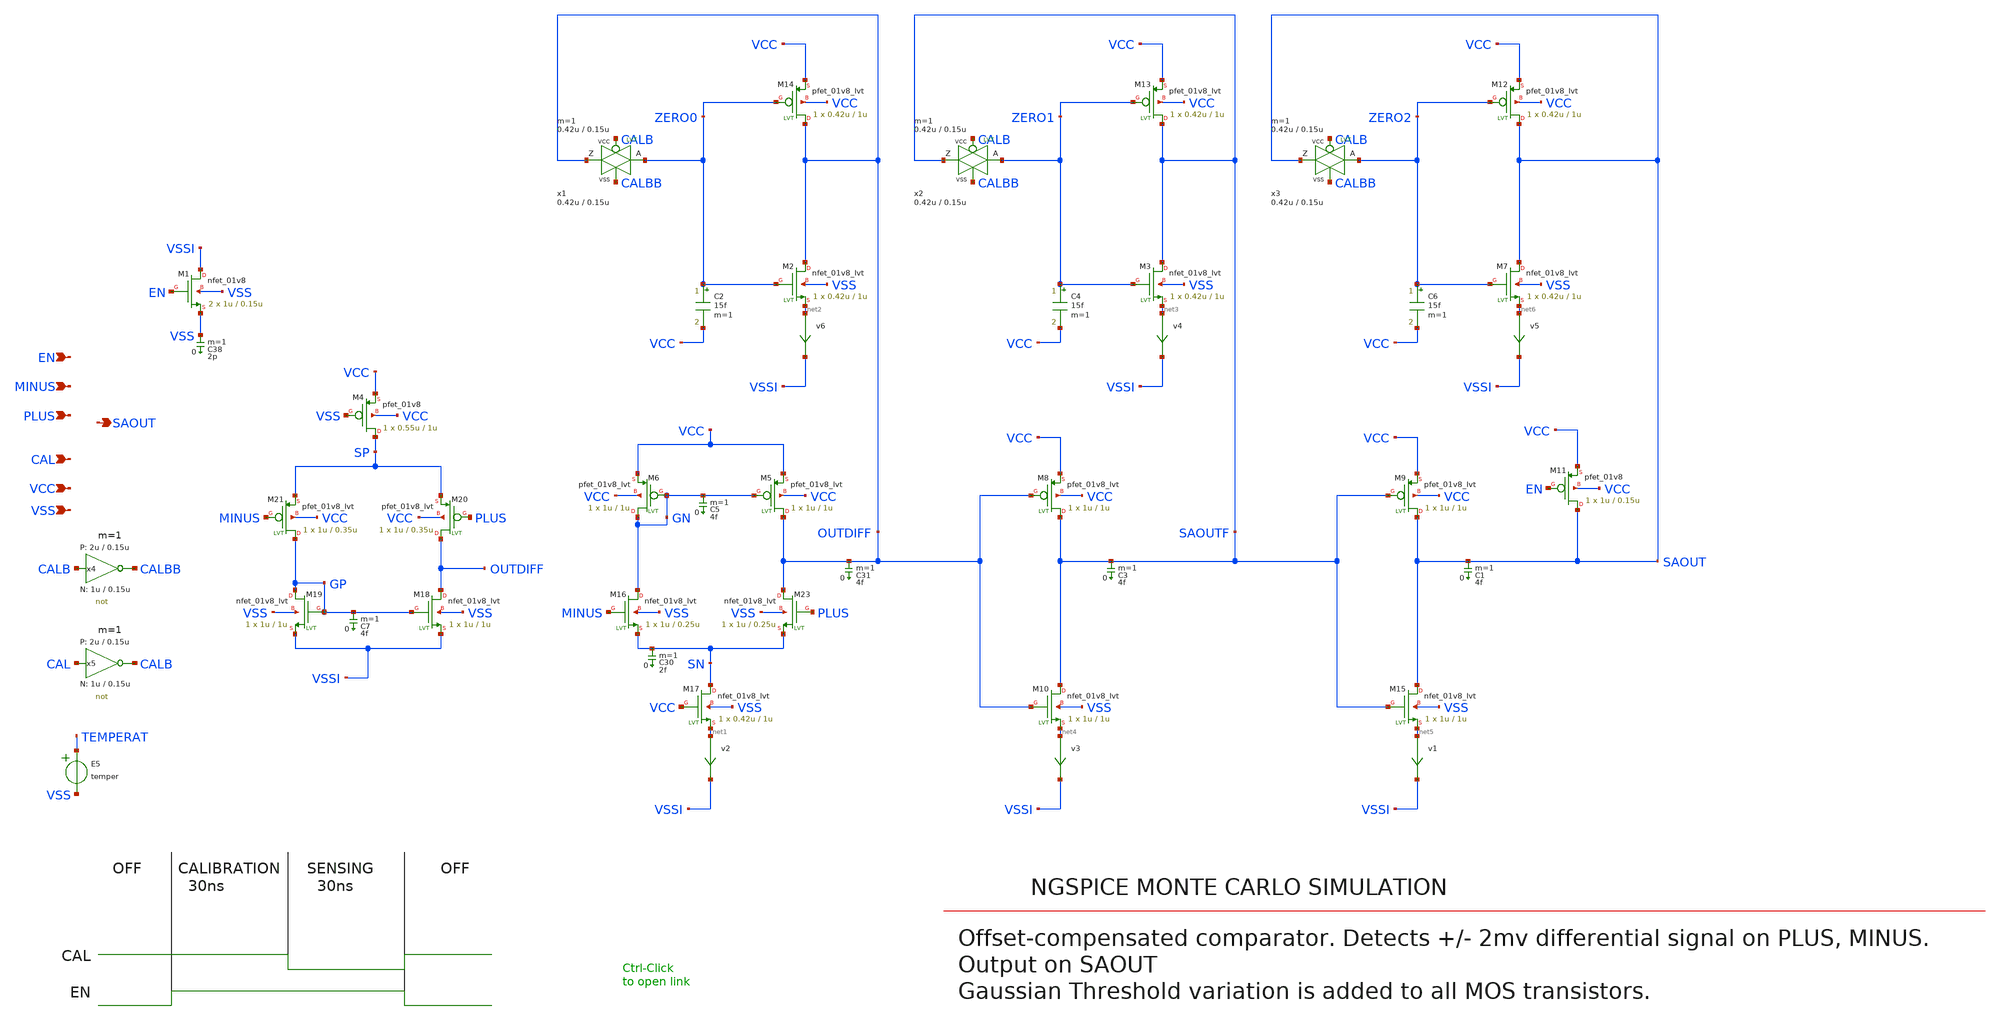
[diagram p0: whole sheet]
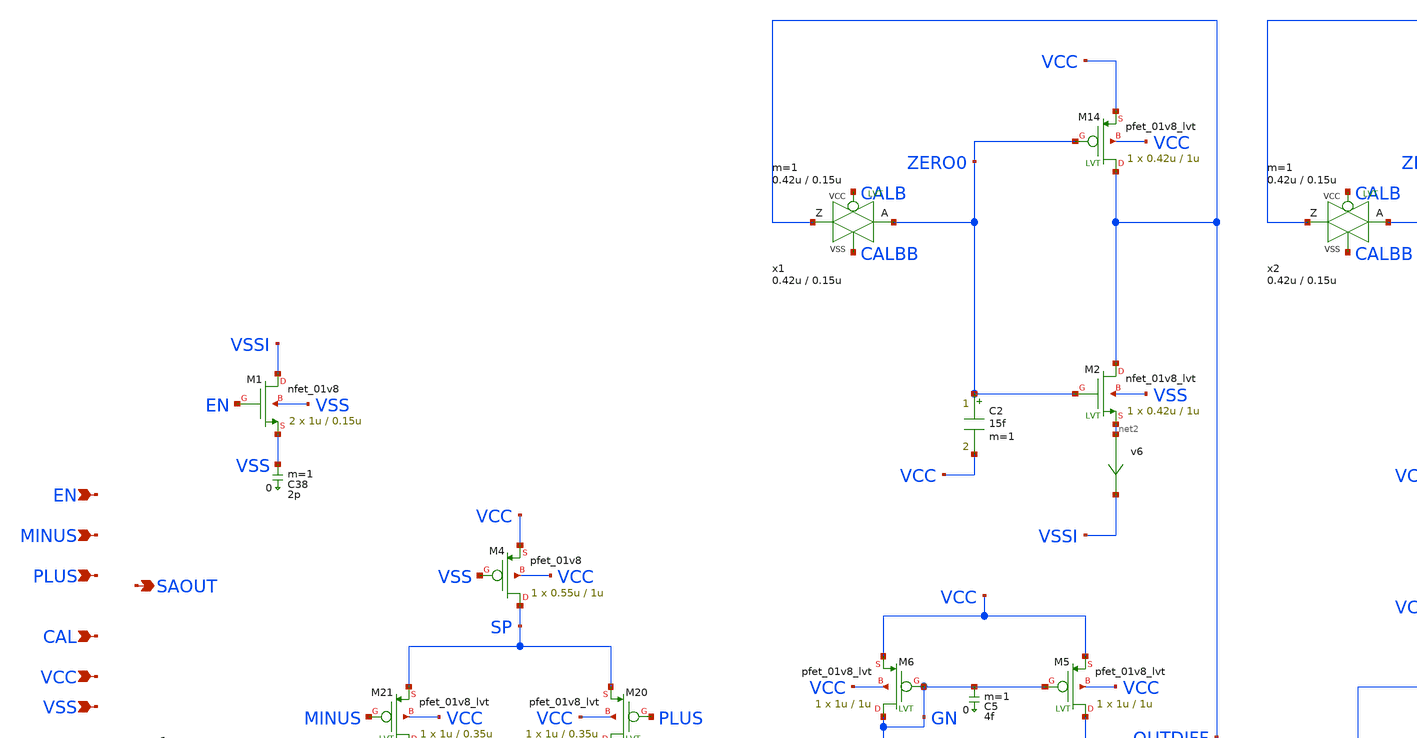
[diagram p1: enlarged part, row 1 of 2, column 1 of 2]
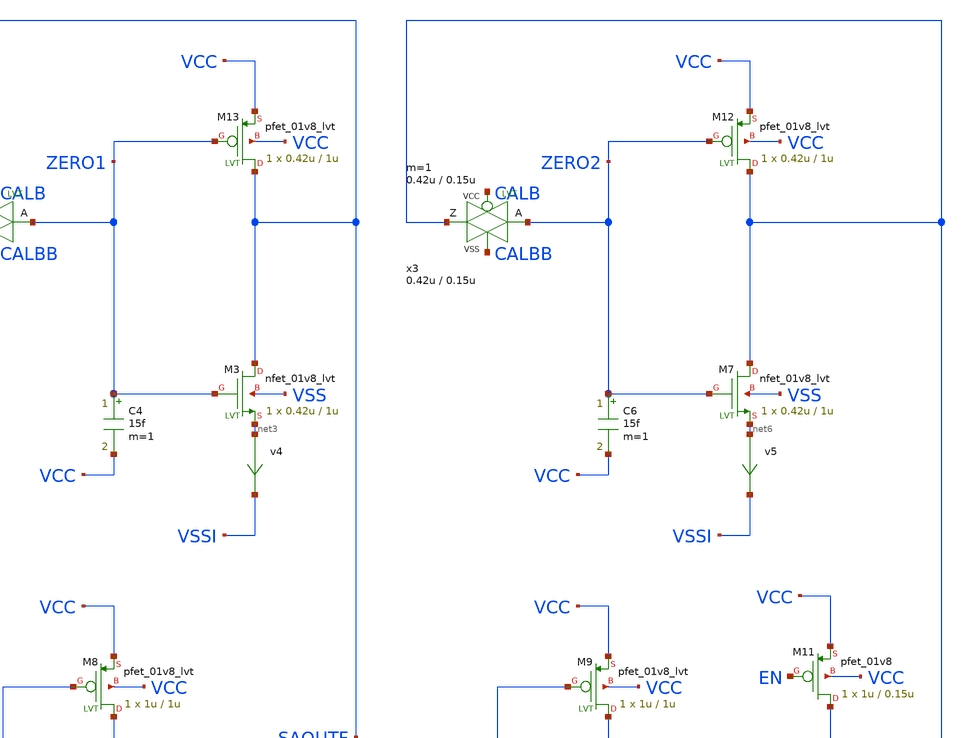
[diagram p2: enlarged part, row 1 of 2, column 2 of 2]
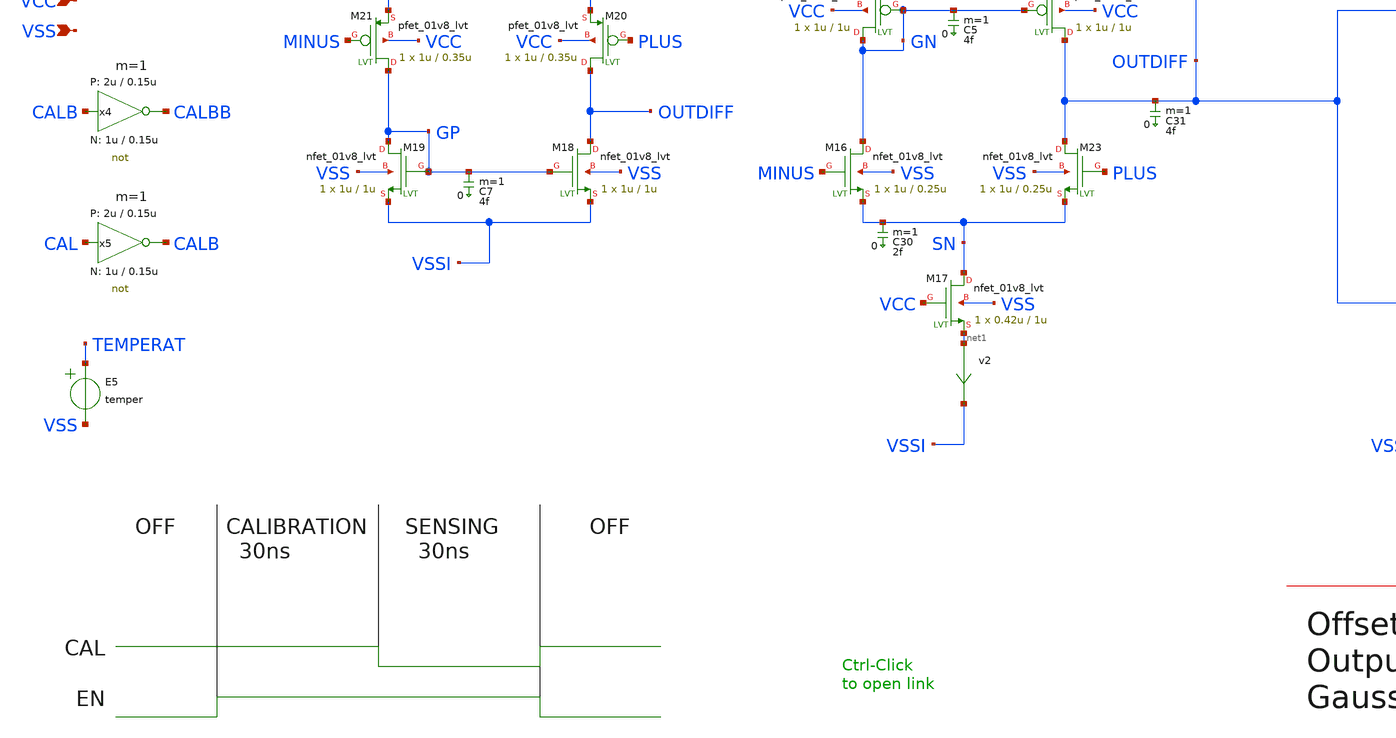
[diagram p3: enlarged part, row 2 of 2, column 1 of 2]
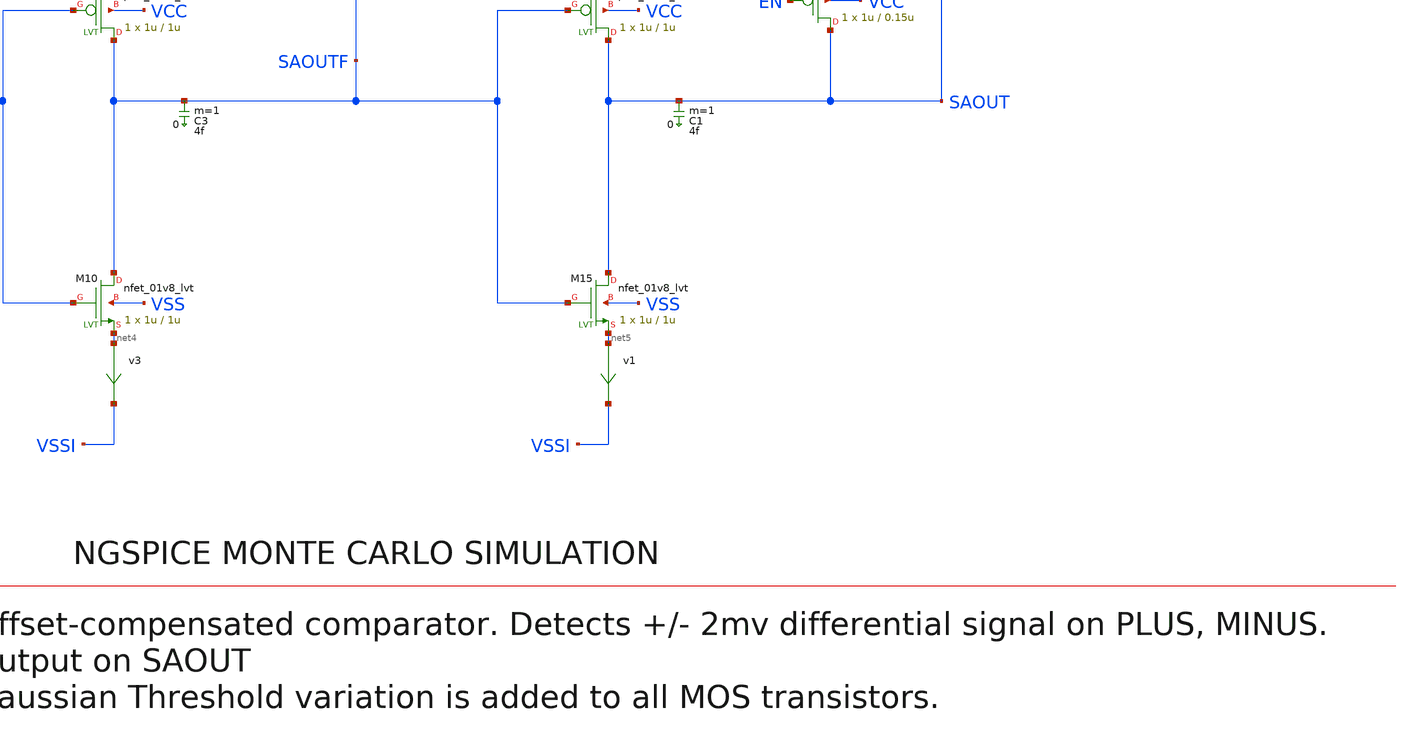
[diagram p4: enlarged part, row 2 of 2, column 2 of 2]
** sch_path: sky130_tests_X/test_comparator.sch
* Copyright 2020 Stefan Frederik Schippers
* Licensed under the Apache License, Version 2.0 (the "License");
* you may not use this file except in compliance with the License.
* You may obtain a copy of the License at
* https://www.apache.org/licenses/LICENSE-2.0
* Unless required by applicable law or agreed to in writing, software
* distributed under the License is distributed on an "AS IS" BASIS,
* WITHOUT WARRANTIES OR CONDITIONS OF ANY KIND, either express or implied.
* See the License for the specific language governing permissions and
* limitations under the License.
* StefanSchippers/xschem_sky130/sky130_tests/not.sch:
* Copyright 2021 Stefan Frederik Schippers
**.subckt test_comparator CAL PLUS MINUS EN VSS VCC SAOUT
*.ipin CAL
*.ipin PLUS
*.ipin MINUS
*.ipin EN
*.ipin VSS
*.ipin VCC
*.opin SAOUT
E5 TEMPERAT VSS VOL=' temper '
C38 VSS 0 2p m=1
C3 SAOUTF 0 4f m=1
C5 GN 0 4f m=1
C30 SN 0 2f m=1
C31 OUTDIFF 0 4f m=1
v2 net1 VSSI 0
.save i(v2)
v3 net4 VSSI 0
.save i(v3)
v4 net3 VSSI 0
.save i(v4)
v6 net2 VSSI 0
.save i(v6)
C1 SAOUT 0 4f m=1
v1 net5 VSSI 0
.save i(v1)
v5 net6 VSSI 0
.save i(v5)
C7 GP 0 4f m=1
x4 CALBB CALB VCC VSS not W_N=1u L_N=0.15u W_P=2u L_P=0.15u m=1
x5 CALB CAL VCC VSS not W_N=1u L_N=0.15u W_P=2u L_P=0.15u m=1
XM4 SP VSS VCC VCC sky130_fd_pr__pfet_01v8 w=0.55u l=1u ad='w * 0.29u' pd='w + 2 * 0.29u' as='w * 0.29u'
+ ps='w + 2 * 0.29u' nrd=0 nrs=0 sa=0 sb=0 sd=0 nf=1 mult=1 m=1
XM5 OUTDIFF GN VCC VCC sky130_fd_pr__pfet_01v8_lvt w=1u l=1u ad='w * 0.29u' pd='2*(w + 0.29u)' as='w * 0.29u'
+ ps='2*(w + 0.29u)' nrd=0 nrs=0 sa=0 sb=0 sd=0 nf=1 mult=1 m=1
XM6 GN GN VCC VCC sky130_fd_pr__pfet_01v8_lvt w=1u l=1u ad='w * 0.29u' pd='2*(w + 0.29u)' as='w * 0.29u'
+ ps='2*(w + 0.29u)' nrd=0 nrs=0 sa=0 sb=0 sd=0 nf=1 mult=1 m=1
XM8 SAOUTF OUTDIFF VCC VCC sky130_fd_pr__pfet_01v8_lvt w=1u l=1u ad='w * 0.29u' pd='2*(w + 0.29u)' as='w * 0.29u'
+ ps='2*(w + 0.29u)' nrd=0 nrs=0 sa=0 sb=0 sd=0 nf=1 mult=1 m=1
XM9 SAOUT SAOUTF VCC VCC sky130_fd_pr__pfet_01v8_lvt w=1u l=1u ad='w * 0.29u' pd='2*(w + 0.29u)' as='w * 0.29u'
+ ps='2*(w + 0.29u)' nrd=0 nrs=0 sa=0 sb=0 sd=0 nf=1 mult=1 m=1
XM11 SAOUT EN VCC VCC sky130_fd_pr__pfet_01v8 w=1u l=0.15u ad='w * 0.29u' pd='w + 2 * 0.29u' as='w * 0.29u'
+ ps='w + 2 * 0.29u' nrd=0 nrs=0 sa=0 sb=0 sd=0 nf=1 mult=1 m=1
XM12 SAOUT ZERO2 VCC VCC sky130_fd_pr__pfet_01v8_lvt w=0.42u l=1u ad='w * 0.29u' pd='2*(w + 0.29u)' as='w * 0.29u'
+ ps='2*(w + 0.29u)' nrd=0 nrs=0 sa=0 sb=0 sd=0 nf=1 mult=1 m=1
XM13 SAOUTF ZERO1 VCC VCC sky130_fd_pr__pfet_01v8_lvt w=0.42u l=1u ad='w * 0.29u' pd='2*(w + 0.29u)'
+ as='w * 0.29u' ps='2*(w + 0.29u)' nrd=0 nrs=0 sa=0 sb=0 sd=0 nf=1 mult=1 m=1
XM14 OUTDIFF ZERO0 VCC VCC sky130_fd_pr__pfet_01v8_lvt w=0.42u l=1u ad='w * 0.29u' pd='2*(w + 0.29u)'
+ as='w * 0.29u' ps='2*(w + 0.29u)' nrd=0 nrs=0 sa=0 sb=0 sd=0 nf=1 mult=1 m=1
XM1 VSSI EN VSS VSS sky130_fd_pr__nfet_01v8 w=1u l=0.15u ad='w * 0.29u' pd='w + 2 * 0.29u' as='w * 0.29u'
+ ps='w + 2 * 0.29u' nrd=0 nrs=0 sa=0 sb=0 sd=0 nf=1 mult=2 m=2
XM2 OUTDIFF ZERO0 net2 VSS sky130_fd_pr__nfet_01v8_lvt w=0.42u l=1u ad='w * 0.29u' pd='2*(w + 0.29u)'
+ as='w * 0.29u' ps='2*(w + 0.29u)' nrd=0 nrs=0 sa=0 sb=0 sd=0 nf=1 mult=1 m=1
XM3 SAOUTF ZERO1 net3 VSS sky130_fd_pr__nfet_01v8_lvt w=0.42u l=1u ad='w * 0.29u' pd='2*(w + 0.29u)'
+ as='w * 0.29u' ps='2*(w + 0.29u)' nrd=0 nrs=0 sa=0 sb=0 sd=0 nf=1 mult=1 m=1
XM7 SAOUT ZERO2 net6 VSS sky130_fd_pr__nfet_01v8_lvt w=0.42u l=1u ad='w * 0.29u' pd='2*(w + 0.29u)' as='w * 0.29u'
+ ps='2*(w + 0.29u)' nrd=0 nrs=0 sa=0 sb=0 sd=0 nf=1 mult=1 m=1
XM15 SAOUT SAOUTF net5 VSS sky130_fd_pr__nfet_01v8_lvt w=1u l=1u ad='w * 0.29u' pd='2*(w + 0.29u)' as='w * 0.29u'
+ ps='2*(w + 0.29u)' nrd=0 nrs=0 sa=0 sb=0 sd=0 nf=1 mult=1 m=1
XM10 SAOUTF OUTDIFF net4 VSS sky130_fd_pr__nfet_01v8_lvt w=1u l=1u ad='w * 0.29u' pd='2*(w + 0.29u)'
+ as='w * 0.29u' ps='2*(w + 0.29u)' nrd=0 nrs=0 sa=0 sb=0 sd=0 nf=1 mult=1 m=1
XM17 SN VCC net1 VSS sky130_fd_pr__nfet_01v8_lvt w=0.42u l=1u ad='w * 0.29u' pd='2*(w + 0.29u)' as='w * 0.29u'
+ ps='2*(w + 0.29u)' nrd=0 nrs=0 sa=0 sb=0 sd=0 nf=1 mult=1 m=1
XM18 OUTDIFF GP VSSI VSS sky130_fd_pr__nfet_01v8_lvt w=1u l=1u ad='w * 0.29u' pd='2*(w + 0.29u)' as='w * 0.29u'
+ ps='2*(w + 0.29u)' nrd=0 nrs=0 sa=0 sb=0 sd=0 nf=1 mult=1 m=1
XM19 GP GP VSSI VSS sky130_fd_pr__nfet_01v8_lvt w=1u l=1u ad='w * 0.29u' pd='2*(w + 0.29u)' as='w * 0.29u'
+ ps='2*(w + 0.29u)' nrd=0 nrs=0 sa=0 sb=0 sd=0 nf=1 mult=1 m=1
XM20 OUTDIFF PLUS SP VCC sky130_fd_pr__pfet_01v8_lvt w=1u l=0.35u ad='w * 0.29u' pd='2*(w + 0.29u)' as='w * 0.29u'
+ ps='2*(w + 0.29u)' nrd=0 nrs=0 sa=0 sb=0 sd=0 nf=1 mult=1 m=1
XM21 GP MINUS SP VCC sky130_fd_pr__pfet_01v8_lvt w=1u l=0.35u ad='w * 0.29u' pd='2*(w + 0.29u)' as='w * 0.29u'
+ ps='2*(w + 0.29u)' nrd=0 nrs=0 sa=0 sb=0 sd=0 nf=1 mult=1 m=1
XM23 OUTDIFF PLUS SN VSS sky130_fd_pr__nfet_01v8_lvt w=1u l=0.25u ad='w * 0.29u' pd='2*(w + 0.29u)' as='w * 0.29u'
+ ps='2*(w + 0.29u)' nrd=0 nrs=0 sa=0 sb=0 sd=0 nf=1 mult=1 m=1
XM16 GN MINUS SN VSS sky130_fd_pr__nfet_01v8_lvt w=1u l=0.25u ad='w * 0.29u' pd='2*(w + 0.29u)' as='w * 0.29u'
+ ps='2*(w + 0.29u)' nrd=0 nrs=0 sa=0 sb=0 sd=0 nf=1 mult=1 m=1
x1 OUTDIFF ZERO0 CALB CALBB VCC VSS passgate_nlvt W_N=0.42u L_N=0.15u W_P=0.42u L_P=0.15u m=1
x2 SAOUTF ZERO1 CALB CALBB VCC VSS passgate_nlvt W_N=0.42u L_N=0.15u W_P=0.42u L_P=0.15u m=1
x3 SAOUT ZERO2 CALB CALBB VCC VSS passgate_nlvt W_N=0.42u L_N=0.15u W_P=0.42u L_P=0.15u m=1
C2 ZERO0 VCC 15f m=1
C4 ZERO1 VCC 15f m=1
C6 ZERO2 VCC 15f m=1
**** begin user architecture code

**** end user architecture code
**.ends

* expanding   symbol:  sky130_tests/not.sym # of pins=2
** sym_path: sky130_tests/not.sym
** sch_path: sky130_tests/not.sch
.subckt not y a VCCPIN VSSPIN     W_N=1 L_N=0.15 W_P=2 L_P=0.15
*.opin y
*.ipin a
XM1 DN a VSSPIN VSSPIN sky130_fd_pr__nfet_01v8 w=W_N l=L_N ad=[sky130_fet_ad_cb W_N ]
+ pd=[sky130_fet_pd_cb W_N ] as=[sky130_fet_ad_cb W_N ] ps=[sky130_fet_pd_cb W_N ] nrd=[sky130_fet_nrd_cb W_N ]
+ nrs=[sky130_fet_nrd_cb W_N ] sa=0 sb=0 sd=0 nf=1 mult=1 m=1
XM2 DP a VCCPIN VCCPIN sky130_fd_pr__pfet_01v8 w=W_P l=L_P ad=[sky130_fet_ad_cb W_P ]
+ pd=[sky130_fet_pd_cb W_P ] as=[sky130_fet_ad_cb W_P ] ps=[sky130_fet_pd_cb W_P ] nrd=[sky130_fet_nrd_cb W_P ]
+ nrs=[sky130_fet_nrd_cb W_P ] sa=0 sb=0 sd=0 nf=1 mult=1 m=1
Vmeas DP y 0
.save i(vmeas)
Vmeas1 y DN 0
.save i(vmeas1)
.save v(dp)
.save v(dn)
.ends


* expanding   symbol:  sky130_tests/passgate_nlvt.sym # of pins=4
** sym_path: sky130_tests/passgate_nlvt.sym
** sch_path: sky130_tests/passgate_nlvt.sch
.subckt passgate_nlvt Z A GP GN VCCBPIN VSSBPIN  W_N=1 L_N=0.35 W_P=1 L_P=0.35
*.iopin A
*.iopin Z
*.ipin GP
*.ipin GN
XM1 net1 GN net2 VSS sky130_fd_pr__nfet_01v8_lvt w=W_N l=L_N ad=ad pd=pd as=as ps=ps nrd=0 nrs=0
+ sa=0 sb=0 sd=0 nf=1 mult=1 m=1
XM2 A GP Z VCC sky130_fd_pr__pfet_01v8 W=W_P L=L_P ad=ad pd=pd as=as ps=ps nrd=0 nrs=0 sa=0 sb=0
+ sd=0 nf=1 mult=1
.ends

**** begin user architecture code

* .option SCALE=1e-6
.option method=gear seed=12

* this experimental option enables mos model bin
* selection based on W/NF instead of W
.option wnflag=1

.param VCC=1.8
.param VCCGAUSS=agauss(1.8, 0.05, 1)
.param VCC=VCCGAUSS
.param VDL='VCC/2+0.2'
.param ABSVAR=0.02
.temp 25

** to generate following file:
** copy .../xschem_sky130/sky130_tests/stimuli.test_comparator to simulation directory
** then do 'Simulation->Utile Stimuli Editor (GUI)' and press 'Translate'
.include "stimuli_test_comparator.cir"

** variation marameters:
.param sky130_fd_pr__nfet_01v8_lvt__vth0_slope_spectre='agauss(0, ABSVAR, 3)/sky130_fd_pr__nfet_01v8_lvt__vth0_slope'
.param sky130_fd_pr__pfet_01v8_lvt__vth0_slope_spectre='agauss(0, ABSVAR, 3)/sky130_fd_pr__pfet_01v8_lvt__vth0_slope'

* .tran 0.1n 900n uic

.control
  let run=1

  dowhile run <= 20
    if run > 1
      reset
      set appendwrite
    end
    * save saout cal i(vvcc) en plus minus
    tran 0.1n 300n uic
    write test_comparator.raw
    let run = run + 1
  end
.endc


**** end user architecture code
.end
